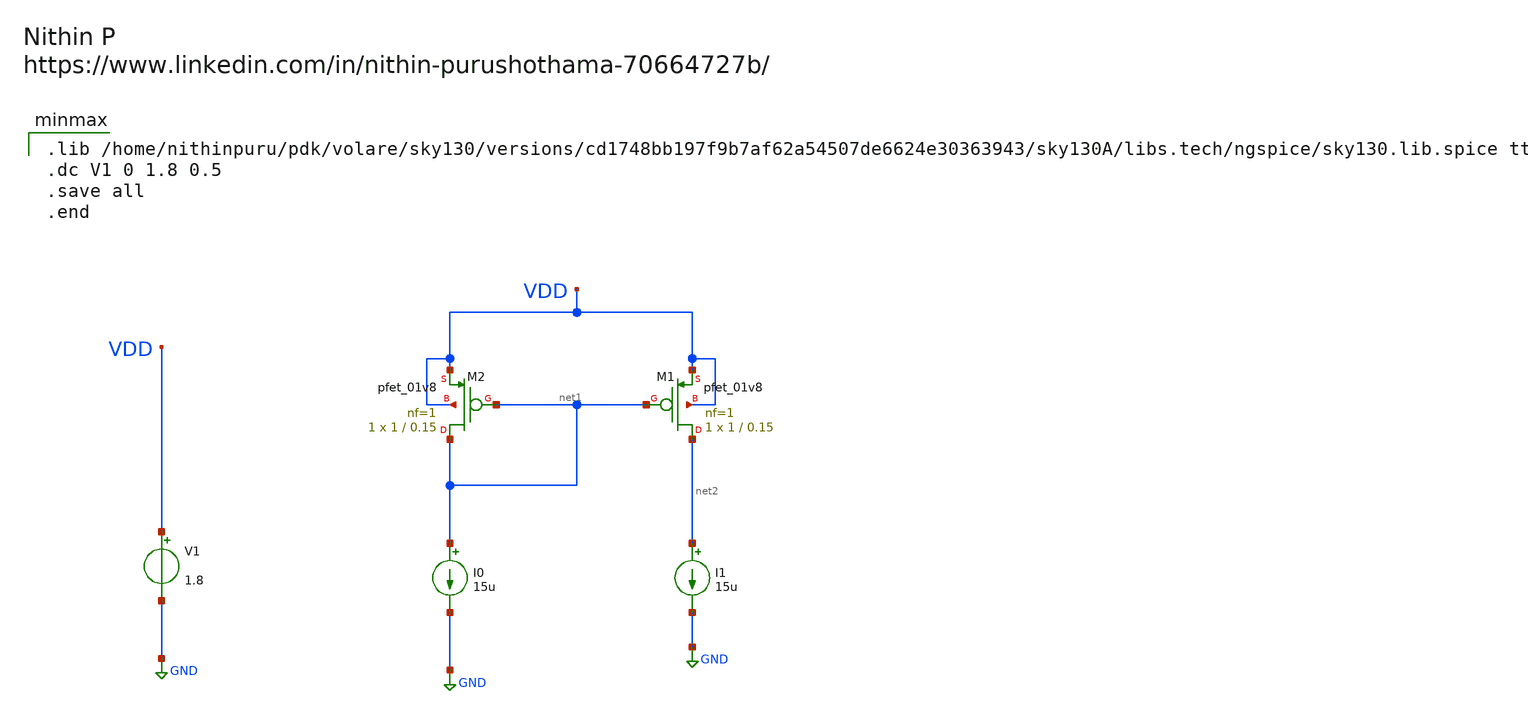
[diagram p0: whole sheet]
** sch_path: Schematics/PMOS Vth Calculation/minmaxPMOS.sch
**.subckt minmaxPMOS
V1 VDD GND 1.8
I0 net1 GND 15u
I1 net2 GND 15u
XM1 net2 net1 VDD VDD sky130_fd_pr__pfet_01v8 L=0.15 W=1 nf=1 ad='int((nf+1)/2) * W/nf * 0.29' as='int((nf+2)/2) * W/nf * 0.29'
+ pd='2*int((nf+1)/2) * (W/nf + 0.29)' ps='2*int((nf+2)/2) * (W/nf + 0.29)' nrd='0.29 / W' nrs='0.29 / W'
+ sa=0 sb=0 sd=0 mult=1 m=1
XM2 net1 net1 VDD VDD sky130_fd_pr__pfet_01v8 L=0.15 W=1 nf=1 ad='int((nf+1)/2) * W/nf * 0.29' as='int((nf+2)/2) * W/nf * 0.29'
+ pd='2*int((nf+1)/2) * (W/nf + 0.29)' ps='2*int((nf+2)/2) * (W/nf + 0.29)' nrd='0.29 / W' nrs='0.29 / W'
+ sa=0 sb=0 sd=0 mult=1 m=1
**** begin user architecture code

.lib /home/nithinpuru/pdk/volare/sky130/versions/cd1748bb197f9b7af62a54507de6624e30363943/sky130A/libs.tech/ngspice/sky130.lib.spice tt
.dc V1 0 1.8 0.5
.save all
.end

**** end user architecture code
**.ends
.GLOBAL GND
.end
